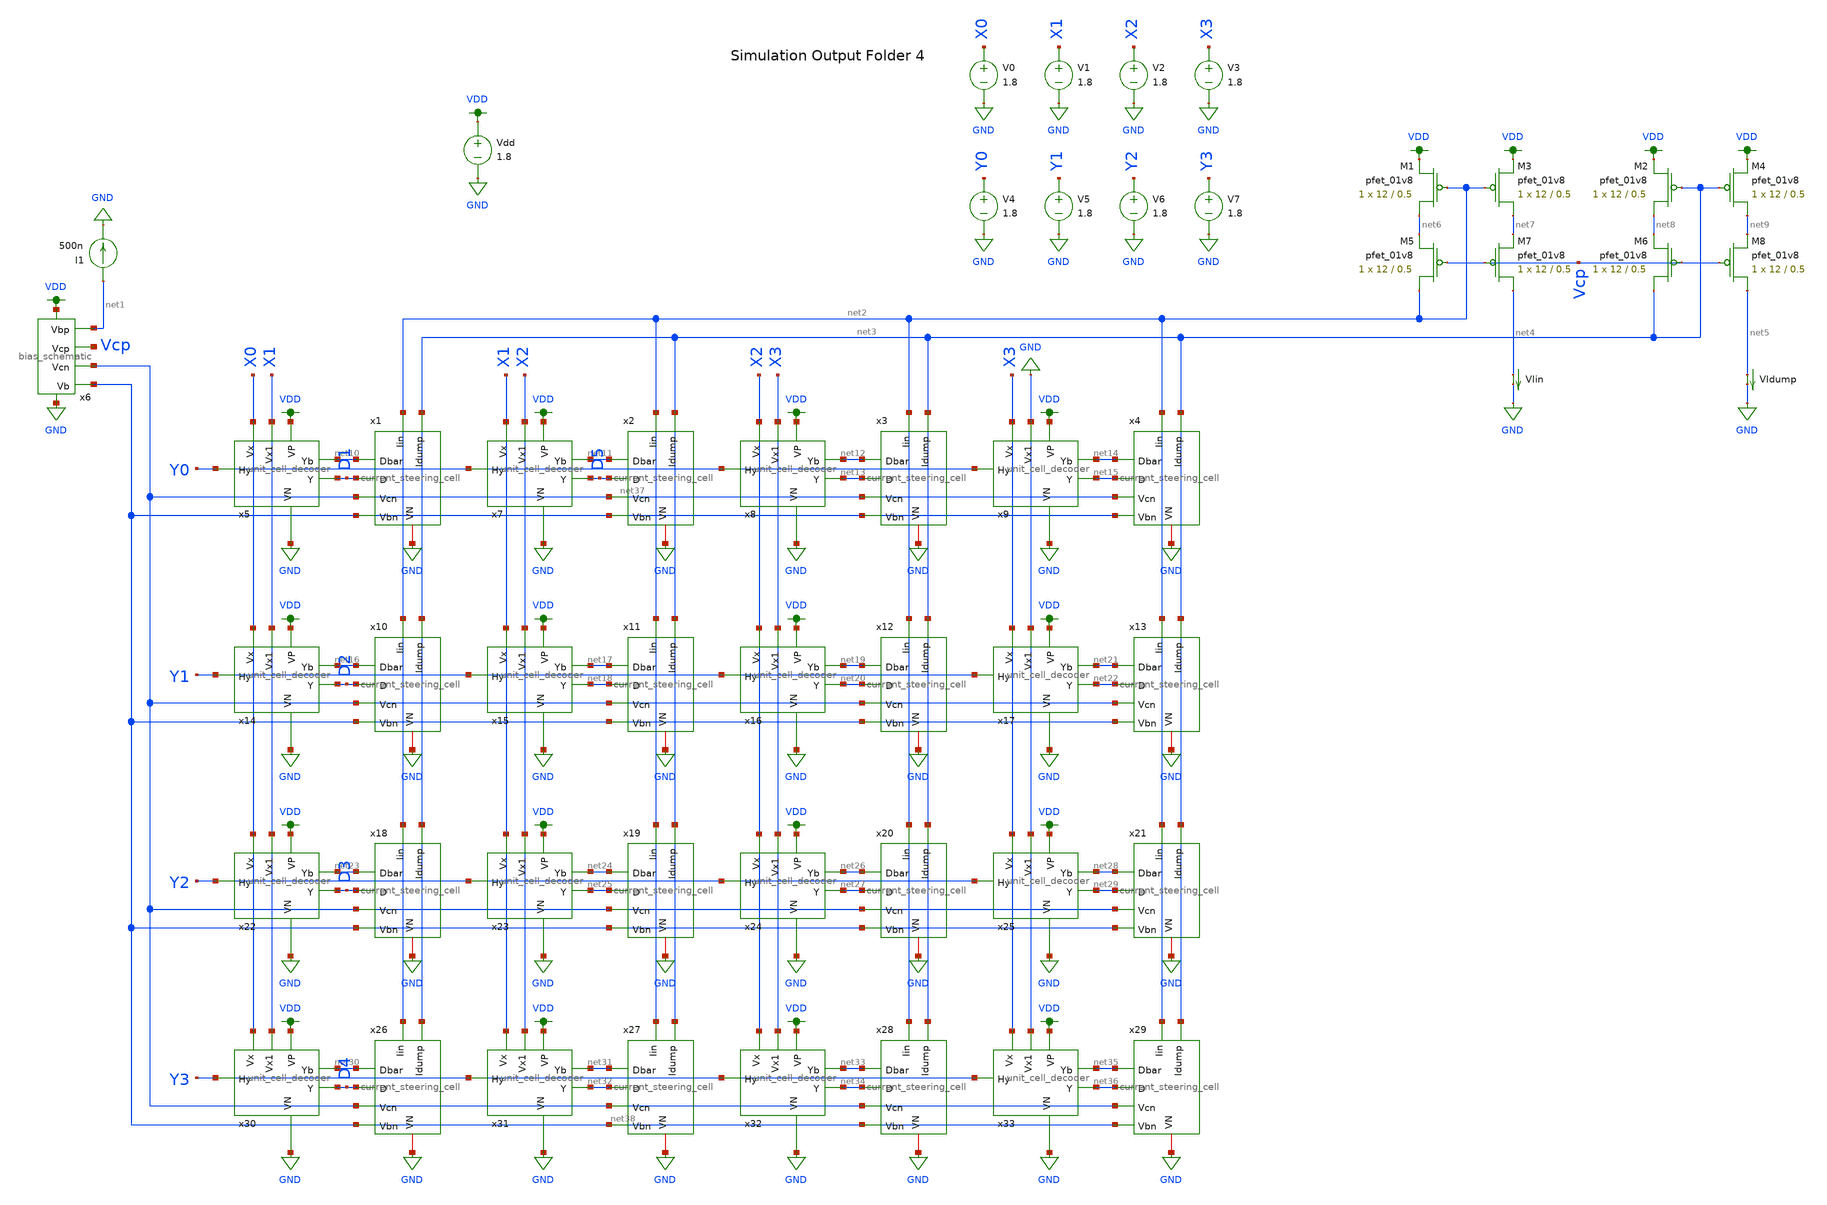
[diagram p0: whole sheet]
** sch_path: xschem/current_steering_testbenches/current_steering_testbench_with_decoder.sch
**.subckt current_steering_testbench_with_decoder
V1 X1 GND 1.8
V2 X2 GND 1.8
V3 X3 GND 1.8
V4 Y0 GND 1.8
I1 net1 GND 500n
VIin net4 GND 0
.save i(viin)
VIdump net5 GND 0
.save i(vidump)
Vdd VDD GND 1.8
XM1 net6 net2 VDD VDD sky130_fd_pr__pfet_01v8 L=0.5 W=12 nf=1 ad='int((nf+1)/2) * W/nf * 0.29' as='int((nf+2)/2) * W/nf * 0.29'
+ pd='2*int((nf+1)/2) * (W/nf + 0.29)' ps='2*int((nf+2)/2) * (W/nf + 0.29)' nrd='0.29 / W' nrs='0.29 / W'
+ sa=0 sb=0 sd=0 mult=1 m=1
XM2 net8 net3 VDD VDD sky130_fd_pr__pfet_01v8 L=0.5 W=12 nf=1 ad='int((nf+1)/2) * W/nf * 0.29' as='int((nf+2)/2) * W/nf * 0.29'
+ pd='2*int((nf+1)/2) * (W/nf + 0.29)' ps='2*int((nf+2)/2) * (W/nf + 0.29)' nrd='0.29 / W' nrs='0.29 / W'
+ sa=0 sb=0 sd=0 mult=1 m=1
XM3 net7 net2 VDD VDD sky130_fd_pr__pfet_01v8 L=0.5 W=12 nf=1 ad='int((nf+1)/2) * W/nf * 0.29' as='int((nf+2)/2) * W/nf * 0.29'
+ pd='2*int((nf+1)/2) * (W/nf + 0.29)' ps='2*int((nf+2)/2) * (W/nf + 0.29)' nrd='0.29 / W' nrs='0.29 / W'
+ sa=0 sb=0 sd=0 mult=1 m=1
XM4 net9 net3 VDD VDD sky130_fd_pr__pfet_01v8 L=0.5 W=12 nf=1 ad='int((nf+1)/2) * W/nf * 0.29' as='int((nf+2)/2) * W/nf * 0.29'
+ pd='2*int((nf+1)/2) * (W/nf + 0.29)' ps='2*int((nf+2)/2) * (W/nf + 0.29)' nrd='0.29 / W' nrs='0.29 / W'
+ sa=0 sb=0 sd=0 mult=1 m=1
XM5 net2 Vcp net6 VDD sky130_fd_pr__pfet_01v8 L=0.5 W=12 nf=1 ad='int((nf+1)/2) * W/nf * 0.29' as='int((nf+2)/2) * W/nf * 0.29'
+ pd='2*int((nf+1)/2) * (W/nf + 0.29)' ps='2*int((nf+2)/2) * (W/nf + 0.29)' nrd='0.29 / W' nrs='0.29 / W'
+ sa=0 sb=0 sd=0 mult=1 m=1
XM6 net3 Vcp net8 VDD sky130_fd_pr__pfet_01v8 L=0.5 W=12 nf=1 ad='int((nf+1)/2) * W/nf * 0.29' as='int((nf+2)/2) * W/nf * 0.29'
+ pd='2*int((nf+1)/2) * (W/nf + 0.29)' ps='2*int((nf+2)/2) * (W/nf + 0.29)' nrd='0.29 / W' nrs='0.29 / W'
+ sa=0 sb=0 sd=0 mult=1 m=1
XM7 net4 Vcp net7 VDD sky130_fd_pr__pfet_01v8 L=0.5 W=12 nf=1 ad='int((nf+1)/2) * W/nf * 0.29' as='int((nf+2)/2) * W/nf * 0.29'
+ pd='2*int((nf+1)/2) * (W/nf + 0.29)' ps='2*int((nf+2)/2) * (W/nf + 0.29)' nrd='0.29 / W' nrs='0.29 / W'
+ sa=0 sb=0 sd=0 mult=1 m=1
XM8 net5 Vcp net9 VDD sky130_fd_pr__pfet_01v8 L=0.5 W=12 nf=1 ad='int((nf+1)/2) * W/nf * 0.29' as='int((nf+2)/2) * W/nf * 0.29'
+ pd='2*int((nf+1)/2) * (W/nf + 0.29)' ps='2*int((nf+2)/2) * (W/nf + 0.29)' nrd='0.29 / W' nrs='0.29 / W'
+ sa=0 sb=0 sd=0 mult=1 m=1
V5 Y1 GND 1.8
V6 Y2 GND 1.8
V7 Y3 GND 1.8
V0 X0 GND 1.8
x5 X0 X1 Y0 VDD GND net10 D1 unit_cell_decoder
x7 X1 X2 Y0 VDD GND net11 D5 unit_cell_decoder
x8 X2 X3 Y0 VDD GND net12 net13 unit_cell_decoder
x9 X3 GND Y0 VDD GND net14 net15 unit_cell_decoder
x14 X0 X1 Y1 VDD GND net16 D2 unit_cell_decoder
x15 X1 X2 Y1 VDD GND net17 net18 unit_cell_decoder
x16 X2 X3 Y1 VDD GND net19 net20 unit_cell_decoder
x17 X3 GND Y1 VDD GND net21 net22 unit_cell_decoder
x22 X0 X1 Y2 VDD GND net23 D3 unit_cell_decoder
x23 X1 X2 Y2 VDD GND net24 net25 unit_cell_decoder
x24 X2 X3 Y2 VDD GND net26 net27 unit_cell_decoder
x25 X3 GND Y2 VDD GND net28 net29 unit_cell_decoder
x30 X0 X1 Y3 VDD GND net30 D4 unit_cell_decoder
x31 X1 X2 Y3 VDD GND net31 net32 unit_cell_decoder
x32 X2 X3 Y3 VDD GND net33 net34 unit_cell_decoder
x33 X3 GND Y3 VDD GND net35 net36 unit_cell_decoder
x1 net2 net3 net10 D1 net37 net38 GND current_steering_cell
x2 net2 net3 net11 D5 net37 net38 GND current_steering_cell
x3 net2 net3 net12 net13 net37 net38 GND current_steering_cell
x4 net2 net3 net14 net15 net37 net38 GND current_steering_cell
x10 net2 net3 net16 D2 net37 net38 GND current_steering_cell
x11 net2 net3 net17 net18 net37 net38 GND current_steering_cell
x12 net2 net3 net19 net20 net37 net38 GND current_steering_cell
x13 net2 net3 net21 net22 net37 net38 GND current_steering_cell
x18 net2 net3 net23 D3 net37 net38 GND current_steering_cell
x19 net2 net3 net24 net25 net37 net38 GND current_steering_cell
x20 net2 net3 net26 net27 net37 net38 GND current_steering_cell
x21 net2 net3 net28 net29 net37 net38 GND current_steering_cell
x26 net2 net3 net30 D4 net37 net38 GND current_steering_cell
x27 net2 net3 net31 net32 net37 net38 GND current_steering_cell
x28 net2 net3 net33 net34 net37 net38 GND current_steering_cell
x29 net2 net3 net35 net36 net37 net38 GND current_steering_cell
x6 VDD net1 Vcp net37 GND net38 bias_schematic
**** begin user architecture code

.save all
.control
set wr_vecnames
set wr_singlescale

let mc_runs = 1
let run = 1
dowhile run <= mc_runs

  let code = 0
  while code <= 16

    if code eq 0
      let y0 = 1 * 1.8
      let y1 = 1 * 1.8
      let y2 = 1 * 1.8
      let y3 = 1 * 1.8
      let x0 = 0 * 1.8
      let x1 = 0 * 1.8
      let x2 = 0 * 1.8
      let x3 = 0 * 1.8
    end
    if code eq 1
      let y0 = 1 * 1.8
      let y1 = 0 * 1.8
      let y2 = 0 * 1.8
      let y3 = 0 * 1.8
      let x0 = 1 * 1.8
      let x1 = 0 * 1.8
      let x2 = 0 * 1.8
      let x3 = 0 * 1.8
    end
    if code eq 2
      let y0 = 1 * 1.8
      let y1 = 1 * 1.8
      let y2 = 0 * 1.8
      let y3 = 0 * 1.8
      let x0 = 1 * 1.8
      let x1 = 0 * 1.8
      let x2 = 0 * 1.8
      let x3 = 0 * 1.8
    end
    if code eq 3
      let y0 = 1 * 1.8
      let y1 = 1 * 1.8
      let y2 = 1 * 1.8
      let y3 = 0 * 1.8
      let x0 = 1 * 1.8
      let x1 = 0 * 1.8
      let x2 = 0 * 1.8
      let x3 = 0 * 1.8
    end
    if code eq 4
      let y0 = 1 * 1.8
      let y1 = 1 * 1.8
      let y2 = 1 * 1.8
      let y3 = 1 * 1.8
      let x0 = 1 * 1.8
      let x1 = 0 * 1.8
      let x2 = 0 * 1.8
      let x3 = 0 * 1.8
    end
    if code eq 5
      let y0 = 1 * 1.8
      let y1 = 0 * 1.8
      let y2 = 0 * 1.8
      let y3 = 0 * 1.8
      let x0 = 1 * 1.8
      let x1 = 1 * 1.8
      let x2 = 0 * 1.8
      let x3 = 0 * 1.8
    end
    if code eq 6
      let y0 = 1 * 1.8
      let y1 = 1 * 1.8
      let y2 = 0 * 1.8
      let y3 = 0 * 1.8
      let x0 = 1 * 1.8
      let x1 = 1 * 1.8
      let x2 = 0 * 1.8
      let x3 = 0 * 1.8
    end
    if code eq 7
      let y0 = 1 * 1.8
      let y1 = 1 * 1.8
      let y2 = 1 * 1.8
      let y3 = 0 * 1.8
      let x0 = 1 * 1.8
      let x1 = 1 * 1.8
      let x2 = 0 * 1.8
      let x3 = 0 * 1.8
    end
    if code eq 8
      let y0 = 1 * 1.8
      let y1 = 1 * 1.8
      let y2 = 1 * 1.8
      let y3 = 1 * 1.8
      let x0 = 1 * 1.8
      let x1 = 1 * 1.8
      let x2 = 0 * 1.8
      let x3 = 0 * 1.8
    end
    if code eq 9
      let y0 = 1 * 1.8
      let y1 = 0 * 1.8
      let y2 = 0 * 1.8
      let y3 = 0 * 1.8
      let x0 = 1 * 1.8
      let x1 = 1 * 1.8
      let x2 = 1 * 1.8
      let x3 = 0 * 1.8
    end
    if code eq 10
      let y0 = 1 * 1.8
      let y1 = 1 * 1.8
      let y2 = 0 * 1.8
      let y3 = 0 * 1.8
      let x0 = 1 * 1.8
      let x1 = 1 * 1.8
      let x2 = 1 * 1.8
      let x3 = 0 * 1.8
    end
    if code eq 11
      let y0 = 1 * 1.8
      let y1 = 1 * 1.8
      let y2 = 1 * 1.8
      let y3 = 0 * 1.8
      let x0 = 1 * 1.8
      let x1 = 1 * 1.8
      let x2 = 1 * 1.8
      let x3 = 0 * 1.8
    end
    if code eq 12
      let y0 = 1 * 1.8
      let y1 = 1 * 1.8
      let y2 = 1 * 1.8
      let y3 = 1 * 1.8
      let x0 = 1 * 1.8
      let x1 = 1 * 1.8
      let x2 = 1 * 1.8
      let x3 = 0 * 1.8
    end
    if code eq 13
      let y0 = 1 * 1.8
      let y1 = 0 * 1.8
      let y2 = 0 * 1.8
      let y3 = 0 * 1.8
      let x0 = 1 * 1.8
      let x1 = 1 * 1.8
      let x2 = 1 * 1.8
      let x3 = 1 * 1.8
    end
    if code eq 14
      let y0 = 1 * 1.8
      let y1 = 1 * 1.8
      let y2 = 0 * 1.8
      let y3 = 0 * 1.8
      let x0 = 1 * 1.8
      let x1 = 1 * 1.8
      let x2 = 1 * 1.8
      let x3 = 1 * 1.8
    end
    if code eq 15
      let y0 = 1 * 1.8
      let y1 = 1 * 1.8
      let y2 = 1 * 1.8
      let y3 = 0 * 1.8
      let x0 = 1 * 1.8
      let x1 = 1 * 1.8
      let x2 = 1 * 1.8
      let x3 = 1 * 1.8
    end
    if code eq 16
      let y0 = 1 * 1.8
      let y1 = 1 * 1.8
      let y2 = 1 * 1.8
      let y3 = 1 * 1.8
      let x0 = 1 * 1.8
      let x1 = 1 * 1.8
      let x2 = 1 * 1.8
      let x3 = 1 * 1.8
    end

    alter V0 $&x0
    alter V1 $&x1
    alter V2 $&x2
    alter V3 $&x3
    alter V4 $&y0
    alter V5 $&y1
    alter V6 $&y2
    alter V7 $&y3


    save all
    op

    wrdata ~/dev/git/magic-dds/simulations/current_steering_dac/4/ieeeDAC_{$&run}.txt code v(D1) v(D2)
+ v(D3) v(D4) v(D5) i(VIin) i(VIdump)
    if code eq 0
      set appendwrite
      set wr_vecnames = FALSE
    end
    let code = code + 1
  end
  reset
  set appendwrite = FALSE
  set wr_vecnames
  let run = run + 1
end
.endc


.option wnflag=1
.param MC_SWITCH=0.0
.lib ~/skywater/skywater-pdk/libraries/sky130_fd_pr_ngspice/latest/models/sky130.lib.spice tt

**** end user architecture code
**.ends
.GLOBAL GND
.GLOBAL VDD
.end
